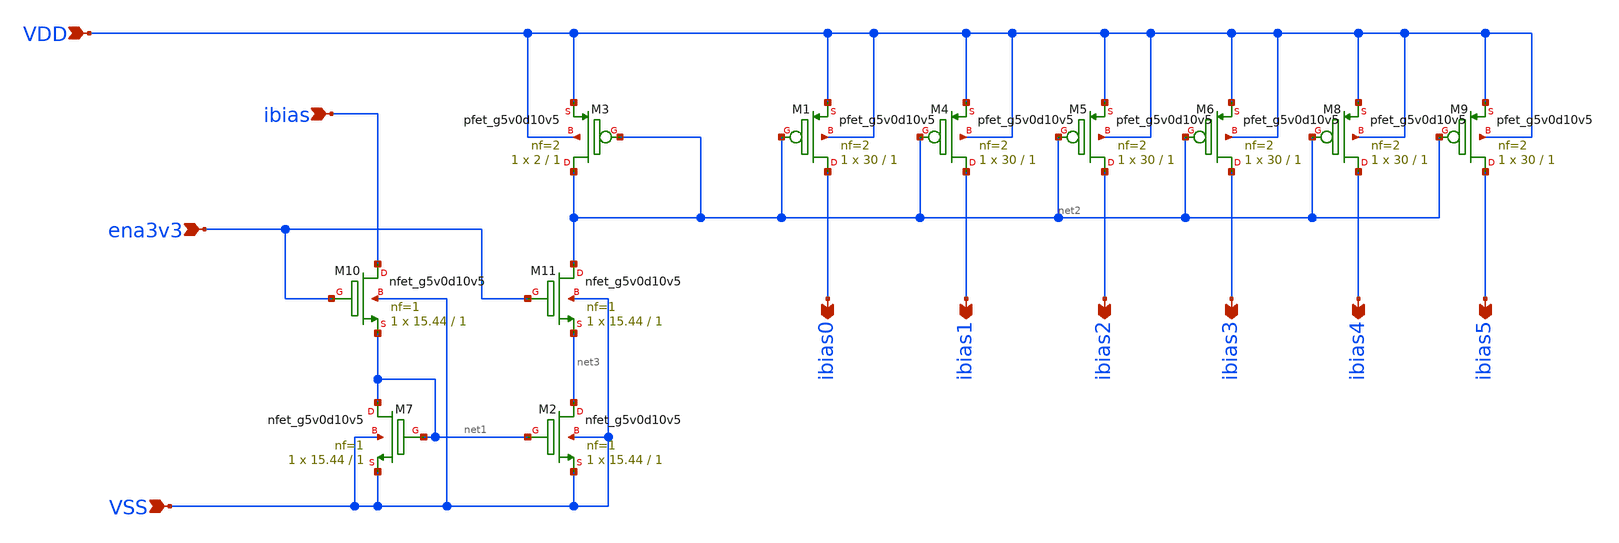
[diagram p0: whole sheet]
** sch_path: xschem/amp_biases.sch
**.subckt amp_biases VSS VDD ibias ena3v3 ibias0 ibias1 ibias2 ibias3 ibias4 ibias5
*.ipin VSS
*.ipin VDD
*.ipin ibias
*.ipin ena3v3
*.opin ibias0
*.opin ibias1
*.opin ibias2
*.opin ibias3
*.opin ibias4
*.opin ibias5
XM1 ibias0 net2 VDD VDD sky130_fd_pr__pfet_g5v0d10v5 L=1 W=30 nf=2 ad='int((nf+1)/2) * W/nf * 0.29' as='int((nf+2)/2) * W/nf * 0.29'
+ pd='2*int((nf+1)/2) * (W/nf + 0.29)' ps='2*int((nf+2)/2) * (W/nf + 0.29)' nrd='0.29 / W' nrs='0.29 / W'
+ sa=0 sb=0 sd=0 mult=1 m=1
XM7 net1 net1 VSS VSS sky130_fd_pr__nfet_g5v0d10v5 L=1 W=15.44 nf=1 ad='int((nf+1)/2) * W/nf * 0.29'
+ as='int((nf+2)/2) * W/nf * 0.29' pd='2*int((nf+1)/2) * (W/nf + 0.29)' ps='2*int((nf+2)/2) * (W/nf + 0.29)'
+ nrd='0.29 / W' nrs='0.29 / W' sa=0 sb=0 sd=0 mult=1 m=1
XM3 net2 net2 VDD VDD sky130_fd_pr__pfet_g5v0d10v5 L=1 W=2 nf=2 ad='int((nf+1)/2) * W/nf * 0.29' as='int((nf+2)/2) * W/nf * 0.29'
+ pd='2*int((nf+1)/2) * (W/nf + 0.29)' ps='2*int((nf+2)/2) * (W/nf + 0.29)' nrd='0.29 / W' nrs='0.29 / W'
+ sa=0 sb=0 sd=0 mult=1 m=1
XM2 net3 net1 VSS VSS sky130_fd_pr__nfet_g5v0d10v5 L=1 W=15.44 nf=1 ad='int((nf+1)/2) * W/nf * 0.29'
+ as='int((nf+2)/2) * W/nf * 0.29' pd='2*int((nf+1)/2) * (W/nf + 0.29)' ps='2*int((nf+2)/2) * (W/nf + 0.29)'
+ nrd='0.29 / W' nrs='0.29 / W' sa=0 sb=0 sd=0 mult=1 m=1
XM4 ibias1 net2 VDD VDD sky130_fd_pr__pfet_g5v0d10v5 L=1 W=30 nf=2 ad='int((nf+1)/2) * W/nf * 0.29' as='int((nf+2)/2) * W/nf * 0.29'
+ pd='2*int((nf+1)/2) * (W/nf + 0.29)' ps='2*int((nf+2)/2) * (W/nf + 0.29)' nrd='0.29 / W' nrs='0.29 / W'
+ sa=0 sb=0 sd=0 mult=1 m=1
XM5 ibias2 net2 VDD VDD sky130_fd_pr__pfet_g5v0d10v5 L=1 W=30 nf=2 ad='int((nf+1)/2) * W/nf * 0.29' as='int((nf+2)/2) * W/nf * 0.29'
+ pd='2*int((nf+1)/2) * (W/nf + 0.29)' ps='2*int((nf+2)/2) * (W/nf + 0.29)' nrd='0.29 / W' nrs='0.29 / W'
+ sa=0 sb=0 sd=0 mult=1 m=1
XM6 ibias3 net2 VDD VDD sky130_fd_pr__pfet_g5v0d10v5 L=1 W=30 nf=2 ad='int((nf+1)/2) * W/nf * 0.29' as='int((nf+2)/2) * W/nf * 0.29'
+ pd='2*int((nf+1)/2) * (W/nf + 0.29)' ps='2*int((nf+2)/2) * (W/nf + 0.29)' nrd='0.29 / W' nrs='0.29 / W'
+ sa=0 sb=0 sd=0 mult=1 m=1
XM8 ibias4 net2 VDD VDD sky130_fd_pr__pfet_g5v0d10v5 L=1 W=30 nf=2 ad='int((nf+1)/2) * W/nf * 0.29' as='int((nf+2)/2) * W/nf * 0.29'
+ pd='2*int((nf+1)/2) * (W/nf + 0.29)' ps='2*int((nf+2)/2) * (W/nf + 0.29)' nrd='0.29 / W' nrs='0.29 / W'
+ sa=0 sb=0 sd=0 mult=1 m=1
XM9 ibias5 net2 VDD VDD sky130_fd_pr__pfet_g5v0d10v5 L=1 W=30 nf=2 ad='int((nf+1)/2) * W/nf * 0.29' as='int((nf+2)/2) * W/nf * 0.29'
+ pd='2*int((nf+1)/2) * (W/nf + 0.29)' ps='2*int((nf+2)/2) * (W/nf + 0.29)' nrd='0.29 / W' nrs='0.29 / W'
+ sa=0 sb=0 sd=0 mult=1 m=1
XM11 net2 ena3v3 net3 VSS sky130_fd_pr__nfet_g5v0d10v5 L=1 W=15.44 nf=1 ad='int((nf+1)/2) * W/nf * 0.29'
+ as='int((nf+2)/2) * W/nf * 0.29' pd='2*int((nf+1)/2) * (W/nf + 0.29)' ps='2*int((nf+2)/2) * (W/nf + 0.29)'
+ nrd='0.29 / W' nrs='0.29 / W' sa=0 sb=0 sd=0 mult=1 m=1
XM10 ibias ena3v3 net1 VSS sky130_fd_pr__nfet_g5v0d10v5 L=1 W=15.44 nf=1 ad='int((nf+1)/2) * W/nf * 0.29'
+ as='int((nf+2)/2) * W/nf * 0.29' pd='2*int((nf+1)/2) * (W/nf + 0.29)' ps='2*int((nf+2)/2) * (W/nf + 0.29)'
+ nrd='0.29 / W' nrs='0.29 / W' sa=0 sb=0 sd=0 mult=1 m=1
**.ends
.end
